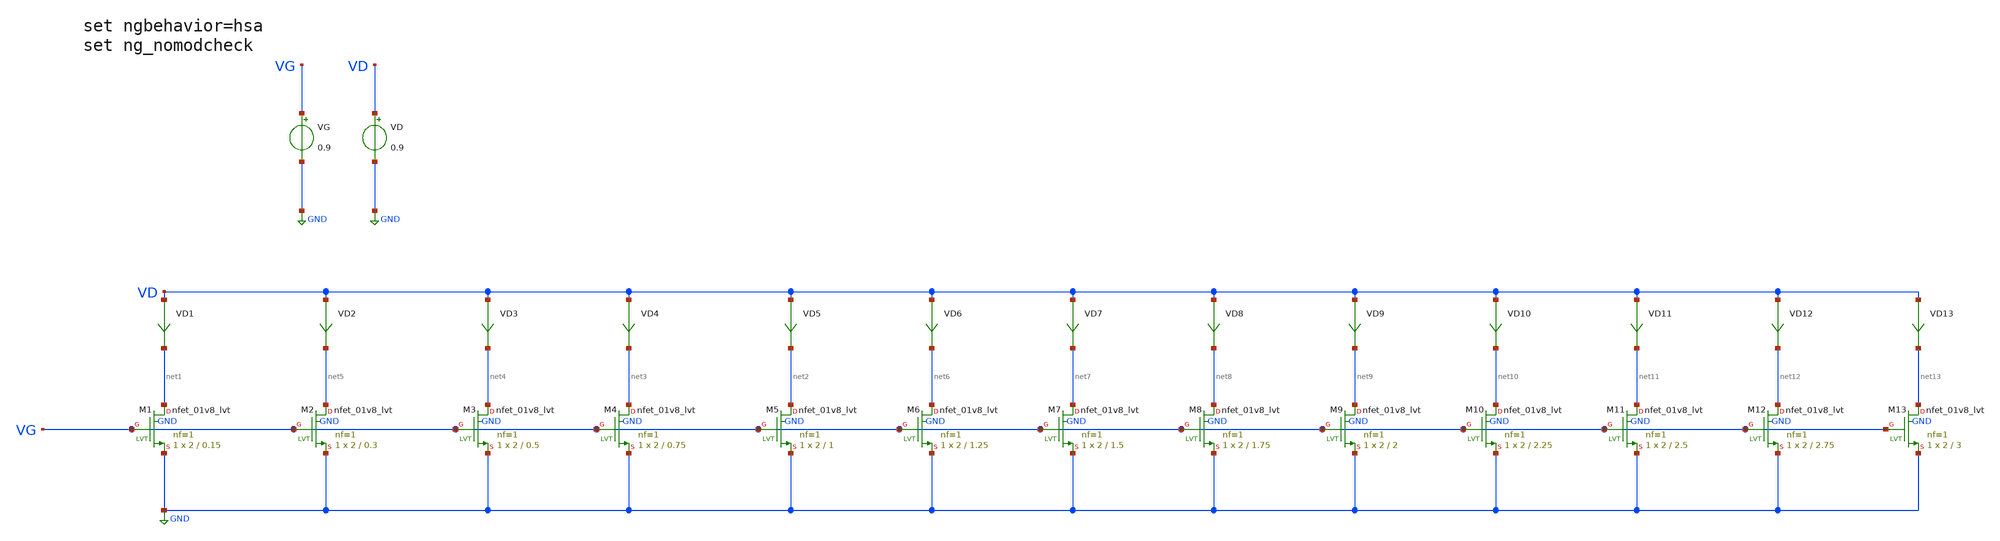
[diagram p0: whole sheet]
** sch_path: Designs/gmid_nmos_1v8_lvt_tb.sch
**.subckt gmid_nmos_1v8_lvt_tb
VG VG GND 0.9
VD VD GND 0.9
VD1 VD net1 0
.save i(vd1)
VD2 VD net5 0
.save i(vd2)
VD3 VD net4 0
.save i(vd3)
VD4 VD net3 0
.save i(vd4)
VD5 VD net2 0
.save i(vd5)
VD6 VD net6 0
.save i(vd6)
VD7 VD net7 0
.save i(vd7)
VD8 VD net8 0
.save i(vd8)
VD9 VD net9 0
.save i(vd9)
VD10 VD net10 0
.save i(vd10)
VD11 VD net11 0
.save i(vd11)
VD12 VD net12 0
.save i(vd12)
VD13 VD net13 0
.save i(vd13)
XM1 net1 VG GND GND sky130_fd_pr__nfet_01v8_lvt L=0.15 W=2 nf=1 ad='int((nf+1)/2) * W/nf * 0.29' as='int((nf+2)/2) * W/nf * 0.29'
+ pd='2*int((nf+1)/2) * (W/nf + 0.29)' ps='2*int((nf+2)/2) * (W/nf + 0.29)' nrd='0.29 / W' nrs='0.29 / W'
+ sa=0 sb=0 sd=0 mult=1 m=1
XM2 net5 VG GND GND sky130_fd_pr__nfet_01v8_lvt L=0.3 W=2 nf=1 ad='int((nf+1)/2) * W/nf * 0.29' as='int((nf+2)/2) * W/nf * 0.29'
+ pd='2*int((nf+1)/2) * (W/nf + 0.29)' ps='2*int((nf+2)/2) * (W/nf + 0.29)' nrd='0.29 / W' nrs='0.29 / W'
+ sa=0 sb=0 sd=0 mult=1 m=1
XM3 net4 VG GND GND sky130_fd_pr__nfet_01v8_lvt L=0.5 W=2 nf=1 ad='int((nf+1)/2) * W/nf * 0.29' as='int((nf+2)/2) * W/nf * 0.29'
+ pd='2*int((nf+1)/2) * (W/nf + 0.29)' ps='2*int((nf+2)/2) * (W/nf + 0.29)' nrd='0.29 / W' nrs='0.29 / W'
+ sa=0 sb=0 sd=0 mult=1 m=1
XM4 net3 VG GND GND sky130_fd_pr__nfet_01v8_lvt L=0.75 W=2 nf=1 ad='int((nf+1)/2) * W/nf * 0.29' as='int((nf+2)/2) * W/nf * 0.29'
+ pd='2*int((nf+1)/2) * (W/nf + 0.29)' ps='2*int((nf+2)/2) * (W/nf + 0.29)' nrd='0.29 / W' nrs='0.29 / W'
+ sa=0 sb=0 sd=0 mult=1 m=1
XM5 net2 VG GND GND sky130_fd_pr__nfet_01v8_lvt L=1 W=2 nf=1 ad='int((nf+1)/2) * W/nf * 0.29' as='int((nf+2)/2) * W/nf * 0.29'
+ pd='2*int((nf+1)/2) * (W/nf + 0.29)' ps='2*int((nf+2)/2) * (W/nf + 0.29)' nrd='0.29 / W' nrs='0.29 / W'
+ sa=0 sb=0 sd=0 mult=1 m=1
XM6 net6 VG GND GND sky130_fd_pr__nfet_01v8_lvt L=1.25 W=2 nf=1 ad='int((nf+1)/2) * W/nf * 0.29' as='int((nf+2)/2) * W/nf * 0.29'
+ pd='2*int((nf+1)/2) * (W/nf + 0.29)' ps='2*int((nf+2)/2) * (W/nf + 0.29)' nrd='0.29 / W' nrs='0.29 / W'
+ sa=0 sb=0 sd=0 mult=1 m=1
XM7 net7 VG GND GND sky130_fd_pr__nfet_01v8_lvt L=1.5 W=2 nf=1 ad='int((nf+1)/2) * W/nf * 0.29' as='int((nf+2)/2) * W/nf * 0.29'
+ pd='2*int((nf+1)/2) * (W/nf + 0.29)' ps='2*int((nf+2)/2) * (W/nf + 0.29)' nrd='0.29 / W' nrs='0.29 / W'
+ sa=0 sb=0 sd=0 mult=1 m=1
XM8 net8 VG GND GND sky130_fd_pr__nfet_01v8_lvt L=1.75 W=2 nf=1 ad='int((nf+1)/2) * W/nf * 0.29' as='int((nf+2)/2) * W/nf * 0.29'
+ pd='2*int((nf+1)/2) * (W/nf + 0.29)' ps='2*int((nf+2)/2) * (W/nf + 0.29)' nrd='0.29 / W' nrs='0.29 / W'
+ sa=0 sb=0 sd=0 mult=1 m=1
XM9 net9 VG GND GND sky130_fd_pr__nfet_01v8_lvt L=2 W=2 nf=1 ad='int((nf+1)/2) * W/nf * 0.29' as='int((nf+2)/2) * W/nf * 0.29'
+ pd='2*int((nf+1)/2) * (W/nf + 0.29)' ps='2*int((nf+2)/2) * (W/nf + 0.29)' nrd='0.29 / W' nrs='0.29 / W'
+ sa=0 sb=0 sd=0 mult=1 m=1
XM10 net10 VG GND GND sky130_fd_pr__nfet_01v8_lvt L=2.25 W=2 nf=1 ad='int((nf+1)/2) * W/nf * 0.29' as='int((nf+2)/2) * W/nf * 0.29'
+ pd='2*int((nf+1)/2) * (W/nf + 0.29)' ps='2*int((nf+2)/2) * (W/nf + 0.29)' nrd='0.29 / W' nrs='0.29 / W'
+ sa=0 sb=0 sd=0 mult=1 m=1
XM11 net11 VG GND GND sky130_fd_pr__nfet_01v8_lvt L=2.5 W=2 nf=1 ad='int((nf+1)/2) * W/nf * 0.29' as='int((nf+2)/2) * W/nf * 0.29'
+ pd='2*int((nf+1)/2) * (W/nf + 0.29)' ps='2*int((nf+2)/2) * (W/nf + 0.29)' nrd='0.29 / W' nrs='0.29 / W'
+ sa=0 sb=0 sd=0 mult=1 m=1
XM12 net12 VG GND GND sky130_fd_pr__nfet_01v8_lvt L=2.75 W=2 nf=1 ad='int((nf+1)/2) * W/nf * 0.29' as='int((nf+2)/2) * W/nf * 0.29'
+ pd='2*int((nf+1)/2) * (W/nf + 0.29)' ps='2*int((nf+2)/2) * (W/nf + 0.29)' nrd='0.29 / W' nrs='0.29 / W'
+ sa=0 sb=0 sd=0 mult=1 m=1
XM13 net13 VG GND GND sky130_fd_pr__nfet_01v8_lvt L=3 W=2 nf=1 ad='int((nf+1)/2) * W/nf * 0.29' as='int((nf+2)/2) * W/nf * 0.29'
+ pd='2*int((nf+1)/2) * (W/nf + 0.29)' ps='2*int((nf+2)/2) * (W/nf + 0.29)' nrd='0.29 / W' nrs='0.29 / W'
+ sa=0 sb=0 sd=0 mult=1 m=1
**** begin user architecture code

** opencircuitdesign pdks install
.lib $::SKYWATER_MODELS/sky130.lib.spice ff




* ngspice commands
.option wnflag=1
.option savecurrents
.control
save all
save @m.xm1.msky130_fd_pr__nfet_01v8_lvt[gm]
save @m.xm2.msky130_fd_pr__nfet_01v8_lvt[gm]
save @m.xm3.msky130_fd_pr__nfet_01v8_lvt[gm]
save @m.xm4.msky130_fd_pr__nfet_01v8_lvt[gm]
save @m.xm5.msky130_fd_pr__nfet_01v8_lvt[gm]
save @m.xm6.msky130_fd_pr__nfet_01v8_lvt[gm]
save @m.xm7.msky130_fd_pr__nfet_01v8_lvt[gm]
save @m.xm8.msky130_fd_pr__nfet_01v8_lvt[gm]
save @m.xm9.msky130_fd_pr__nfet_01v8_lvt[gm]
save @m.xm10.msky130_fd_pr__nfet_01v8_lvt[gm]
save @m.xm11.msky130_fd_pr__nfet_01v8_lvt[gm]
save @m.xm12.msky130_fd_pr__nfet_01v8_lvt[gm]
save @m.xm13.msky130_fd_pr__nfet_01v8_lvt[gm]
save @m.xm1.msky130_fd_pr__nfet_01v8_lvt[id]
save @m.xm2.msky130_fd_pr__nfet_01v8_lvt[id]
save @m.xm3.msky130_fd_pr__nfet_01v8_lvt[id]
save @m.xm4.msky130_fd_pr__nfet_01v8_lvt[id]
save @m.xm5.msky130_fd_pr__nfet_01v8_lvt[id]
save @m.xm6.msky130_fd_pr__nfet_01v8_lvt[id]
save @m.xm7.msky130_fd_pr__nfet_01v8_lvt[id]
save @m.xm8.msky130_fd_pr__nfet_01v8_lvt[id]
save @m.xm9.msky130_fd_pr__nfet_01v8_lvt[id]
save @m.xm10.msky130_fd_pr__nfet_01v8_lvt[id]
save @m.xm11.msky130_fd_pr__nfet_01v8_lvt[id]
save @m.xm12.msky130_fd_pr__nfet_01v8_lvt[id]
save @m.xm13.msky130_fd_pr__nfet_01v8_lvt[id]
save @m.xm1.msky130_fd_pr__nfet_01v8_lvt[vth]
save @m.xm2.msky130_fd_pr__nfet_01v8_lvt[vth]
save @m.xm3.msky130_fd_pr__nfet_01v8_lvt[vth]
save @m.xm4.msky130_fd_pr__nfet_01v8_lvt[vth]
save @m.xm5.msky130_fd_pr__nfet_01v8_lvt[vth]
save @m.xm6.msky130_fd_pr__nfet_01v8_lvt[vth]
save @m.xm7.msky130_fd_pr__nfet_01v8_lvt[vth]
save @m.xm8.msky130_fd_pr__nfet_01v8_lvt[vth]
save @m.xm9.msky130_fd_pr__nfet_01v8_lvt[vth]
save @m.xm10.msky130_fd_pr__nfet_01v8_lvt[vth]
save @m.xm11.msky130_fd_pr__nfet_01v8_lvt[vth]
save @m.xm12.msky130_fd_pr__nfet_01v8_lvt[vth]
save @m.xm13.msky130_fd_pr__nfet_01v8_lvt[vth]
save @m.xm1.msky130_fd_pr__nfet_01v8_lvt[gds]
save @m.xm2.msky130_fd_pr__nfet_01v8_lvt[gds]
save @m.xm3.msky130_fd_pr__nfet_01v8_lvt[gds]
save @m.xm4.msky130_fd_pr__nfet_01v8_lvt[gds]
save @m.xm5.msky130_fd_pr__nfet_01v8_lvt[gds]
save @m.xm6.msky130_fd_pr__nfet_01v8_lvt[gds]
save @m.xm7.msky130_fd_pr__nfet_01v8_lvt[gds]
save @m.xm8.msky130_fd_pr__nfet_01v8_lvt[gds]
save @m.xm9.msky130_fd_pr__nfet_01v8_lvt[gds]
save @m.xm10.msky130_fd_pr__nfet_01v8_lvt[gds]
save @m.xm11.msky130_fd_pr__nfet_01v8_lvt[gds]
save @m.xm12.msky130_fd_pr__nfet_01v8_lvt[gds]
save @m.xm13.msky130_fd_pr__nfet_01v8_lvt[gds]
save @m.xm1.msky130_fd_pr__nfet_01v8_lvt[cgg]
save @m.xm2.msky130_fd_pr__nfet_01v8_lvt[cgg]
save @m.xm3.msky130_fd_pr__nfet_01v8_lvt[cgg]
save @m.xm4.msky130_fd_pr__nfet_01v8_lvt[cgg]
save @m.xm5.msky130_fd_pr__nfet_01v8_lvt[cgg]
save @m.xm6.msky130_fd_pr__nfet_01v8_lvt[cgg]
save @m.xm7.msky130_fd_pr__nfet_01v8_lvt[cgg]
save @m.xm8.msky130_fd_pr__nfet_01v8_lvt[cgg]
save @m.xm9.msky130_fd_pr__nfet_01v8_lvt[cgg]
save @m.xm10.msky130_fd_pr__nfet_01v8_lvt[cgg]
save @m.xm11.msky130_fd_pr__nfet_01v8_lvt[cgg]
save @m.xm12.msky130_fd_pr__nfet_01v8_lvt[cgg]
save @m.xm13.msky130_fd_pr__nfet_01v8_lvt[cgg]
save @m.xm1.msky130_fd_pr__nfet_01v8_lvt[cgs]
save @m.xm2.msky130_fd_pr__nfet_01v8_lvt[cgs]
save @m.xm3.msky130_fd_pr__nfet_01v8_lvt[cgs]
save @m.xm4.msky130_fd_pr__nfet_01v8_lvt[cgs]
save @m.xm5.msky130_fd_pr__nfet_01v8_lvt[cgs]
save @m.xm6.msky130_fd_pr__nfet_01v8_lvt[cgs]
save @m.xm7.msky130_fd_pr__nfet_01v8_lvt[cgs]
save @m.xm8.msky130_fd_pr__nfet_01v8_lvt[cgs]
save @m.xm9.msky130_fd_pr__nfet_01v8_lvt[cgs]
save @m.xm10.msky130_fd_pr__nfet_01v8_lvt[cgs]
save @m.xm11.msky130_fd_pr__nfet_01v8_lvt[cgs]
save @m.xm12.msky130_fd_pr__nfet_01v8_lvt[cgs]
save @m.xm13.msky130_fd_pr__nfet_01v8_lvt[cgs]
save @m.xm1.msky130_fd_pr__nfet_01v8_lvt[cgd]
save @m.xm2.msky130_fd_pr__nfet_01v8_lvt[cgd]
save @m.xm3.msky130_fd_pr__nfet_01v8_lvt[cgd]
save @m.xm4.msky130_fd_pr__nfet_01v8_lvt[cgd]
save @m.xm5.msky130_fd_pr__nfet_01v8_lvt[cgd]
save @m.xm6.msky130_fd_pr__nfet_01v8_lvt[cgd]
save @m.xm7.msky130_fd_pr__nfet_01v8_lvt[cgd]
save @m.xm8.msky130_fd_pr__nfet_01v8_lvt[cgd]
save @m.xm9.msky130_fd_pr__nfet_01v8_lvt[cgd]
save @m.xm10.msky130_fd_pr__nfet_01v8_lvt[cgd]
save @m.xm11.msky130_fd_pr__nfet_01v8_lvt[cgd]
save @m.xm12.msky130_fd_pr__nfet_01v8_lvt[cgd]
save @m.xm13.msky130_fd_pr__nfet_01v8_lvt[cgd]
dc VG 0.05 1.8 0.05
** remove zero length vectors to prevent write errors
remzerovec
write /home/nithinpuru/Desktop/OSIC/xschem/SKY130-sim/gmid_nmos_tb.raw
plot @m.xm1.msky130_fd_pr__nfet_01v8_lvt[gm]
plot @m.xm2.msky130_fd_pr__nfet_01v8_lvt[gm]
plot @m.xm3.msky130_fd_pr__nfet_01v8_lvt[gm]
plot @m.xm4.msky130_fd_pr__nfet_01v8_lvt[gm]
plot @m.xm5.msky130_fd_pr__nfet_01v8_lvt[gm]
plot @m.xm6.msky130_fd_pr__nfet_01v8_lvt[gm]
plot @m.xm7.msky130_fd_pr__nfet_01v8_lvt[gm]
plot @m.xm8.msky130_fd_pr__nfet_01v8_lvt[gm]
plot @m.xm9.msky130_fd_pr__nfet_01v8_lvt[gm]
plot @m.xm10.msky130_fd_pr__nfet_01v8_lvt[gm]
plot @m.xm11.msky130_fd_pr__nfet_01v8_lvt[gm]
plot @m.xm12.msky130_fd_pr__nfet_01v8_lvt[gm]
plot @m.xm13.msky130_fd_pr__nfet_01v8_lvt[gm]
wrdata
+ /home/nithinpuru/Desktop/OSIC/xschem/SKY130-sim/PDK-Characterisation/NMOS_1v8_Lvt/gmid_nmos_1_nfet_01v8_lvt_tb.txt @m.xm1.msky130_fd_pr__nfet_01v8_lvt[gm] i(VD1) @m.xm1.msky130_fd_pr__nfet_01v8_lvt[vth]
+ @m.xm1.msky130_fd_pr__nfet_01v8_lvt[gds] @m.xm1.msky130_fd_pr__nfet_01v8_lvt[cgg] @m.xm1.msky130_fd_pr__nfet_01v8_lvt[cgs]
+ @m.xm1.msky130_fd_pr__nfet_01v8_lvt[cgd]
wrdata
+ /home/nithinpuru/Desktop/OSIC/xschem/SKY130-sim/PDK-Characterisation/NMOS_1v8_Lvt/gmid_nmos_2_nfet_01v8_lvt_tb.txt @m.xm2.msky130_fd_pr__nfet_01v8_lvt[gm] i(VD2) @m.xm2.msky130_fd_pr__nfet_01v8_lvt[vth]
+ @m.xm2.msky130_fd_pr__nfet_01v8_lvt[gds] @m.xm2.msky130_fd_pr__nfet_01v8_lvt[cgg] @m.xm2.msky130_fd_pr__nfet_01v8_lvt[cgs]
+ @m.xm2.msky130_fd_pr__nfet_01v8_lvt[cgd]
wrdata
+ /home/nithinpuru/Desktop/OSIC/xschem/SKY130-sim/PDK-Characterisation/NMOS_1v8_Lvt/gmid_nmos_3_nfet_01v8_lvt_tb.txt @m.xm3.msky130_fd_pr__nfet_01v8_lvt[gm] i(VD3) @m.xm3.msky130_fd_pr__nfet_01v8_lvt[vth]
+ @m.xm3.msky130_fd_pr__nfet_01v8_lvt[gds] @m.xm3.msky130_fd_pr__nfet_01v8_lvt[cgg] @m.xm3.msky130_fd_pr__nfet_01v8_lvt[cgs]
+ @m.xm3.msky130_fd_pr__nfet_01v8_lvt[cgd]
wrdata
+ /home/nithinpuru/Desktop/OSIC/xschem/SKY130-sim/PDK-Characterisation/NMOS_1v8_Lvt/gmid_nmos_4_nfet_01v8_lvt_tb.txt @m.xm4.msky130_fd_pr__nfet_01v8_lvt[gm] i(VD4) @m.xm4.msky130_fd_pr__nfet_01v8_lvt[vth]
+ @m.xm4.msky130_fd_pr__nfet_01v8_lvt[gds] @m.xm4.msky130_fd_pr__nfet_01v8_lvt[cgg] @m.xm4.msky130_fd_pr__nfet_01v8_lvt[cgs]
+ @m.xm4.msky130_fd_pr__nfet_01v8_lvt[cgd]
wrdata
+ /home/nithinpuru/Desktop/OSIC/xschem/SKY130-sim/PDK-Characterisation/NMOS_1v8_Lvt/gmid_nmos_5_nfet_01v8_lvt_tb.txt @m.xm5.msky130_fd_pr__nfet_01v8_lvt[gm] i(VD5) @m.xm5.msky130_fd_pr__nfet_01v8_lvt[vth]
+ @m.xm5.msky130_fd_pr__nfet_01v8_lvt[gds] @m.xm5.msky130_fd_pr__nfet_01v8_lvt[cgg] @m.xm5.msky130_fd_pr__nfet_01v8_lvt[cgs]
+ @m.xm5.msky130_fd_pr__nfet_01v8_lvt[cgd]
wrdata
+ /home/nithinpuru/Desktop/OSIC/xschem/SKY130-sim/PDK-Characterisation/NMOS_1v8_Lvt/gmid_nmos_6_nfet_01v8_lvt_tb.txt @m.xm6.msky130_fd_pr__nfet_01v8_lvt[gm] i(VD6) @m.xm6.msky130_fd_pr__nfet_01v8_lvt[vth]
+ @m.xm6.msky130_fd_pr__nfet_01v8_lvt[gds] @m.xm6.msky130_fd_pr__nfet_01v8_lvt[cgg] @m.xm6.msky130_fd_pr__nfet_01v8_lvt[cgs]
+ @m.xm6.msky130_fd_pr__nfet_01v8_lvt[cgd]
wrdata
+ /home/nithinpuru/Desktop/OSIC/xschem/SKY130-sim/PDK-Characterisation/NMOS_1v8_Lvt/gmid_nmos_7_nfet_01v8_lvt_tb.txt @m.xm7.msky130_fd_pr__nfet_01v8_lvt[gm] i(VD7) @m.xm7.msky130_fd_pr__nfet_01v8_lvt[vth]
+ @m.xm7.msky130_fd_pr__nfet_01v8_lvt[gds] @m.xm7.msky130_fd_pr__nfet_01v8_lvt[cgg] @m.xm7.msky130_fd_pr__nfet_01v8_lvt[cgs]
+ @m.xm7.msky130_fd_pr__nfet_01v8_lvt[cgd]
wrdata
+ /home/nithinpuru/Desktop/OSIC/xschem/SKY130-sim/PDK-Characterisation/NMOS_1v8_Lvt/gmid_nmos_8_nfet_01v8_lvt_tb.txt @m.xm8.msky130_fd_pr__nfet_01v8_lvt[gm] i(VD8) @m.xm8.msky130_fd_pr__nfet_01v8_lvt[vth]
+ @m.xm8.msky130_fd_pr__nfet_01v8_lvt[gds] @m.xm8.msky130_fd_pr__nfet_01v8_lvt[cgg] @m.xm8.msky130_fd_pr__nfet_01v8_lvt[cgs]
+ @m.xm8.msky130_fd_pr__nfet_01v8_lvt[cgd]
wrdata
+ /home/nithinpuru/Desktop/OSIC/xschem/SKY130-sim/PDK-Characterisation/NMOS_1v8_Lvt/gmid_nmos_9_nfet_01v8_lvt_tb.txt @m.xm9.msky130_fd_pr__nfet_01v8_lvt[gm] i(VD9) @m.xm9.msky130_fd_pr__nfet_01v8_lvt[vth]
+ @m.xm9.msky130_fd_pr__nfet_01v8_lvt[gds] @m.xm9.msky130_fd_pr__nfet_01v8_lvt[cgg] @m.xm9.msky130_fd_pr__nfet_01v8_lvt[cgs]
+ @m.xm9.msky130_fd_pr__nfet_01v8_lvt[cgd]
wrdata
+ /home/nithinpuru/Desktop/OSIC/xschem/SKY130-sim/PDK-Characterisation/NMOS_1v8_Lvt/gmid_nmos_10_nfet_01v8_lvt_tb.txt @m.xm10.msky130_fd_pr__nfet_01v8_lvt[gm] i(VD10) @m.xm10.msky130_fd_pr__nfet_01v8_lvt[vth]
+ @m.xm10.msky130_fd_pr__nfet_01v8_lvt[gds] @m.xm10.msky130_fd_pr__nfet_01v8_lvt[cgg] @m.xm10.msky130_fd_pr__nfet_01v8_lvt[cgs]
+ @m.xm10.msky130_fd_pr__nfet_01v8_lvt[cgd]
wrdata
+ /home/nithinpuru/Desktop/OSIC/xschem/SKY130-sim/PDK-Characterisation/NMOS_1v8_Lvt/gmid_nmos_11_nfet_01v8_lvt_tb.txt @m.xm11.msky130_fd_pr__nfet_01v8_lvt[gm] i(VD11) @m.xm11.msky130_fd_pr__nfet_01v8_lvt[vth]
+ @m.xm11.msky130_fd_pr__nfet_01v8_lvt[gds] @m.xm11.msky130_fd_pr__nfet_01v8_lvt[cgg] @m.xm11.msky130_fd_pr__nfet_01v8_lvt[cgs]
+ @m.xm11.msky130_fd_pr__nfet_01v8_lvt[cgd]
wrdata
+ /home/nithinpuru/Desktop/OSIC/xschem/SKY130-sim/PDK-Characterisation/NMOS_1v8_Lvt/gmid_nmos_12_nfet_01v8_lvt_tb.txt @m.xm12.msky130_fd_pr__nfet_01v8_lvt[gm] i(VD12) @m.xm12.msky130_fd_pr__nfet_01v8_lvt[vth]
+ @m.xm12.msky130_fd_pr__nfet_01v8_lvt[gds] @m.xm12.msky130_fd_pr__nfet_01v8_lvt[cgg] @m.xm12.msky130_fd_pr__nfet_01v8_lvt[cgs]
+ @m.xm12.msky130_fd_pr__nfet_01v8_lvt[cgd]
wrdata
+ /home/nithinpuru/Desktop/OSIC/xschem/SKY130-sim/PDK-Characterisation/NMOS_1v8_Lvt/gmid_nmos_13_nfet_01v8_lvt_tb.txt @m.xm13.msky130_fd_pr__nfet_01v8_lvt[gm] i(VD13) @m.xm13.msky130_fd_pr__nfet_01v8_lvt[vth]
+ @m.xm13.msky130_fd_pr__nfet_01v8_lvt[gds] @m.xm13.msky130_fd_pr__nfet_01v8_lvt[cgg] @m.xm13.msky130_fd_pr__nfet_01v8_lvt[cgs]
+ @m.xm13.msky130_fd_pr__nfet_01v8_lvt[cgd]
set appendwrite
op
remzerovec
write /home/nithinpuru/Desktop/OSIC/xschem/SKY130-sim/gmid_nmos_tb.raw
quit 0
.endc


**** end user architecture code
**.ends
.GLOBAL GND
.end
